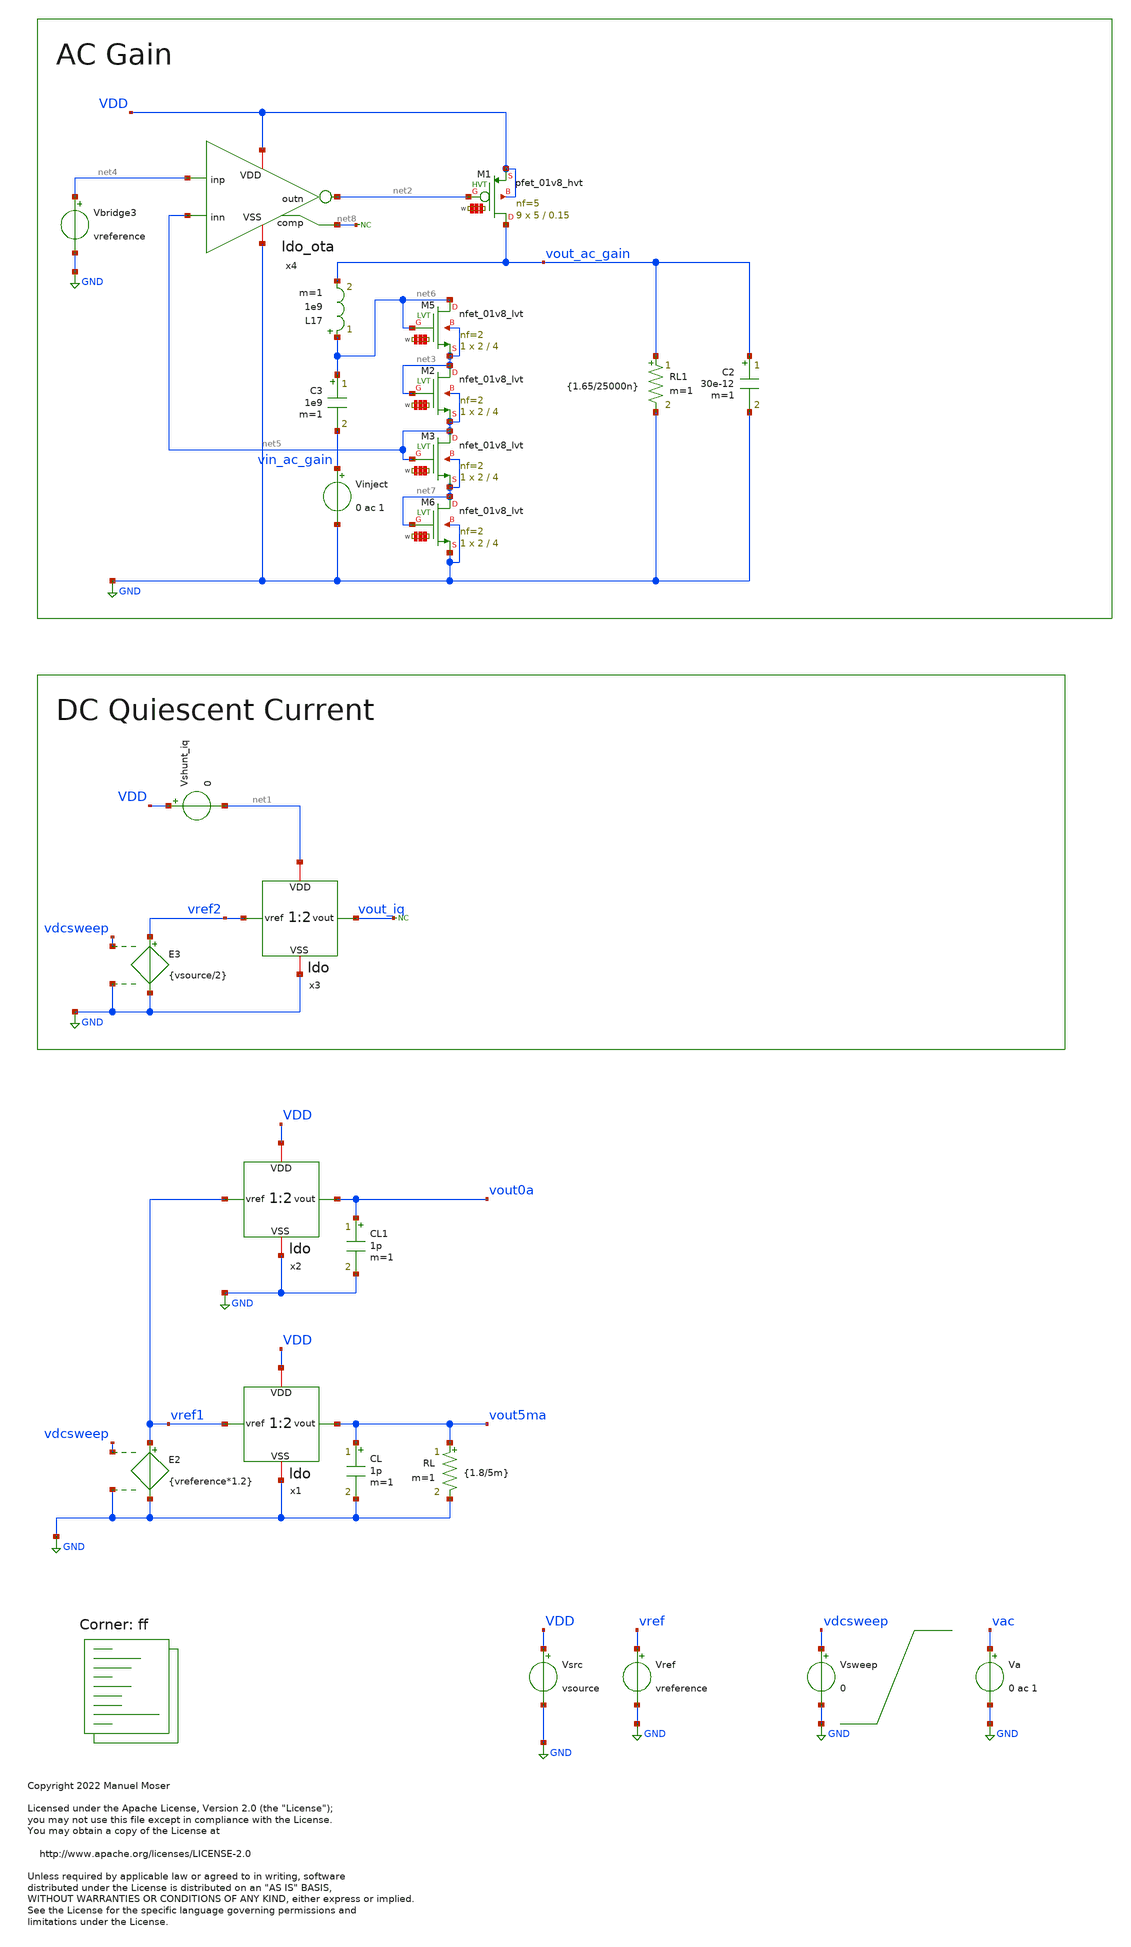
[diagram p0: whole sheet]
** sch_path: xschem/ldo_tb.sch
* Copyright 2022 Manuel Moser
* Licensed under the Apache License, Version 2.0 (the "License");
**.subckt ldo_tb
Vref vref GND vreference
Vsrc VDD GND vsource
Va vac GND 0 ac 1
CL vout5ma GND 1p m=1
RL vout5ma GND {1.8/5m} m=1
x1 VDD vref1 vout5ma GND ldo
CL1 vout0a GND 1p m=1
x2 VDD vref1 vout0a GND ldo
Vsweep vdcsweep GND 0
E2 vref1 GND vdcsweep GND {vreference*1.2}
x3 net1 vref2 vout_iq GND ldo
Vshunt_iq VDD net1 0
E3 vref2 GND vdcsweep GND {vsource/2}
* noconn vout_iq
x4 VDD net4 net2 net5 GND net8 ldo_ota
XM1 vout_ac_gain net2 VDD VDD sky130_fd_pr__pfet_01v8_hvt L=0.15 W='5 * 5 ' nf=5 ad='int((nf+1)/2) * W / nf * 0.29'
+ as='int((nf+2)/2) * W / nf * 0.29' pd='2*int((nf+1)/2) * (W / nf + 0.29)' ps='2*int((nf+2)/2) * (W / nf + 0.29)'
+ nrd='0.29 / W ' nrs='0.29 / W ' sa=0 sb=0 sd=0 mult=9 m=9
XM5 net6 net6 net3 net3 sky130_fd_pr__nfet_01v8_lvt L=4 W='2 * 2 ' nf=2 ad='int((nf+1)/2) * W/nf * 0.29'
+ as='int((nf+2)/2) * W/nf * 0.29' pd='2*int((nf+1)/2) * (W/nf + 0.29)' ps='2*int((nf+2)/2) * (W/nf + 0.29)'
+ nrd='0.29 / W' nrs='0.29 / W' sa=0 sb=0 sd=0 mult=1 m=1
XM2 net3 net3 net5 net5 sky130_fd_pr__nfet_01v8_lvt L=4 W='2 * 2 ' nf=2 ad='int((nf+1)/2) * W/nf * 0.29'
+ as='int((nf+2)/2) * W/nf * 0.29' pd='2*int((nf+1)/2) * (W/nf + 0.29)' ps='2*int((nf+2)/2) * (W/nf + 0.29)'
+ nrd='0.29 / W' nrs='0.29 / W' sa=0 sb=0 sd=0 mult=1 m=1
XM3 net5 net5 net7 net7 sky130_fd_pr__nfet_01v8_lvt L=4 W='2 * 2 ' nf=2 ad='int((nf+1)/2) * W/nf * 0.29'
+ as='int((nf+2)/2) * W/nf * 0.29' pd='2*int((nf+1)/2) * (W/nf + 0.29)' ps='2*int((nf+2)/2) * (W/nf + 0.29)'
+ nrd='0.29 / W' nrs='0.29 / W' sa=0 sb=0 sd=0 mult=1 m=1
XM6 net7 net7 GND GND sky130_fd_pr__nfet_01v8_lvt L=4 W='2 * 2 ' nf=2 ad='int((nf+1)/2) * W/nf * 0.29'
+ as='int((nf+2)/2) * W/nf * 0.29' pd='2*int((nf+1)/2) * (W/nf + 0.29)' ps='2*int((nf+2)/2) * (W/nf + 0.29)'
+ nrd='0.29 / W' nrs='0.29 / W' sa=0 sb=0 sd=0 mult=1 m=1
L17 net6 vout_ac_gain 1e9 m=1
C3 net6 vin_ac_gain 1e9 m=1
Vinject vin_ac_gain GND 0 ac 1
Vbridge3 net4 GND vreference
RL1 vout_ac_gain GND {1.65/25000n} m=1
C2 vout_ac_gain GND 30e-12 m=1
* noconn #net8
**** begin user architecture code



.temp 27
*.option gmin = 1e-16
.option RSHUNT=1E15
.option method = gear

.param vsource = 1.8
.param vdrop = 0.15
.param vreference = {(vsource-vdrop)/2}

.save all
.options savecurrents

.control
set num_threads = 12
write results_ldo.raw
set appendwrite

repeat 1
 reset

dc vsweep 0 1 0.01 temp -30 60 90
write results_ldo.raw   vref1 vout5ma vout0a x1.vota x1.vfb
+ @m.x1.xm5.msky130_fd_pr__nfet_01v8_lvt[id]  vref2 i(vshunt_iq) vout_ac_gain

ac dec 10 1 10meg
write results_ldo.raw vout_ac_gain

*pz vinject gnd vout_ac_gain gnd vol pz


end

.endc




.lib $::SKYWATER_MODELS/sky130.lib.spice ff
**** end user architecture code
**.ends

* expanding   symbol:  ldo.sym # of pins=4
** sym_path: xschem/ldo.sym
** sch_path: xschem/ldo.sch
.subckt ldo VDD vref vout VSS
*.ipin vref
*.iopin VDD
*.iopin VSS
*.opin vout
x1 VDD vref vota vfb VSS ldo_ota
XM1 vout vota VDD VDD sky130_fd_pr__pfet_01v8_hvt L=0.15 W='5 * 5 ' nf=5 ad='int((nf+1)/2) * W / nf * 0.29'
+ as='int((nf+2)/2) * W / nf * 0.29' pd='2*int((nf+1)/2) * (W / nf + 0.29)' ps='2*int((nf+2)/2) * (W / nf + 0.29)'
+ nrd='0.29 / W ' nrs='0.29 / W ' sa=0 sb=0 sd=0 mult=9 m=9
XM5 vout vout net1 net1 sky130_fd_pr__nfet_01v8_lvt L=4 W='2 * 2 ' nf=2 ad='int((nf+1)/2) * W/nf * 0.29'
+ as='int((nf+2)/2) * W/nf * 0.29' pd='2*int((nf+1)/2) * (W/nf + 0.29)' ps='2*int((nf+2)/2) * (W/nf + 0.29)'
+ nrd='0.29 / W' nrs='0.29 / W' sa=0 sb=0 sd=0 mult=1 m=1
XM2 net1 net1 vfb vfb sky130_fd_pr__nfet_01v8_lvt L=4 W='2 * 2 ' nf=2 ad='int((nf+1)/2) * W/nf * 0.29'
+ as='int((nf+2)/2) * W/nf * 0.29' pd='2*int((nf+1)/2) * (W/nf + 0.29)' ps='2*int((nf+2)/2) * (W/nf + 0.29)'
+ nrd='0.29 / W' nrs='0.29 / W' sa=0 sb=0 sd=0 mult=1 m=1
XM3 vfb vfb net2 net2 sky130_fd_pr__nfet_01v8_lvt L=4 W='2 * 2 ' nf=2 ad='int((nf+1)/2) * W/nf * 0.29'
+ as='int((nf+2)/2) * W/nf * 0.29' pd='2*int((nf+1)/2) * (W/nf + 0.29)' ps='2*int((nf+2)/2) * (W/nf + 0.29)'
+ nrd='0.29 / W' nrs='0.29 / W' sa=0 sb=0 sd=0 mult=1 m=1
XM6 net2 net2 VSS VSS sky130_fd_pr__nfet_01v8_lvt L=4 W='2 * 2 ' nf=2 ad='int((nf+1)/2) * W/nf * 0.29'
+ as='int((nf+2)/2) * W/nf * 0.29' pd='2*int((nf+1)/2) * (W/nf + 0.29)' ps='2*int((nf+2)/2) * (W/nf + 0.29)'
+ nrd='0.29 / W' nrs='0.29 / W' sa=0 sb=0 sd=0 mult=1 m=1
.ends


* expanding   symbol:  ldo_ota.sym # of pins=6
** sym_path: xschem/ldo_ota.sym
** sch_path: xschem/ldo_ota.sch
.subckt ldo_ota VDD inp outn inn VSS comp
*.iopin VDD
*.iopin VSS
*.ipin inp
*.ipin inn
*.opin outn
*.opin comp
x2 bias2 VDD VSS bias1 ldo_isource
XM10 net1 bias2 VDD VDD sky130_fd_pr__pfet_01v8_lvt L=8 W='0.55 * 1 ' nf=1 ad='int((nf+1)/2) * W / nf * 0.29'
+ as='int((nf+2)/2) * W / nf * 0.29' pd='2*int((nf+1)/2) * (W / nf + 0.29)' ps='2*int((nf+2)/2) * (W / nf + 0.29)'
+ nrd='0.29 / W ' nrs='0.29 / W ' sa=0 sb=0 sd=0 mult=1 m=1
XM12 bias2 bias2 net1 VDD sky130_fd_pr__pfet_01v8_lvt L=1 W='3 * 3 ' nf=3 ad='int((nf+1)/2) * W / nf * 0.29'
+ as='int((nf+2)/2) * W / nf * 0.29' pd='2*int((nf+1)/2) * (W / nf + 0.29)' ps='2*int((nf+2)/2) * (W / nf + 0.29)'
+ nrd='0.29 / W ' nrs='0.29 / W ' sa=0 sb=0 sd=0 mult=1 m=1
XM1 net2 bias1 VDD VDD sky130_fd_pr__pfet_01v8_lvt L=8 W='0.55 * 4 ' nf=4 ad='int((nf+1)/2) * W / nf * 0.29'
+ as='int((nf+2)/2) * W / nf * 0.29' pd='2*int((nf+1)/2) * (W / nf + 0.29)' ps='2*int((nf+2)/2) * (W / nf + 0.29)'
+ nrd='0.29 / W ' nrs='0.29 / W ' sa=0 sb=0 sd=0 mult=1 m=1
XM2 bias1 bias2 net2 VDD sky130_fd_pr__pfet_01v8_lvt L=1 W='3 * 3 ' nf=3 ad='int((nf+1)/2) * W / nf * 0.29'
+ as='int((nf+2)/2) * W / nf * 0.29' pd='2*int((nf+1)/2) * (W / nf + 0.29)' ps='2*int((nf+2)/2) * (W / nf + 0.29)'
+ nrd='0.29 / W ' nrs='0.29 / W ' sa=0 sb=0 sd=0 mult=1 m=1
XM3 net3 bias1 VDD VDD sky130_fd_pr__pfet_01v8_lvt L=8 W='0.55 * 4 ' nf=4 ad='int((nf+1)/2) * W / nf * 0.29'
+ as='int((nf+2)/2) * W / nf * 0.29' pd='2*int((nf+1)/2) * (W / nf + 0.29)' ps='2*int((nf+2)/2) * (W / nf + 0.29)'
+ nrd='0.29 / W ' nrs='0.29 / W ' sa=0 sb=0 sd=0 mult=1 m=1
XM4 bias3 bias2 net3 VDD sky130_fd_pr__pfet_01v8_lvt L=1 W='3 * 3 ' nf=3 ad='int((nf+1)/2) * W / nf * 0.29'
+ as='int((nf+2)/2) * W / nf * 0.29' pd='2*int((nf+1)/2) * (W / nf + 0.29)' ps='2*int((nf+2)/2) * (W / nf + 0.29)'
+ nrd='0.29 / W ' nrs='0.29 / W ' sa=0 sb=0 sd=0 mult=1 m=1
XM5 net4 bias1 VDD VDD sky130_fd_pr__pfet_01v8_lvt L=8 W='0.55 * 4 ' nf=4 ad='int((nf+1)/2) * W / nf * 0.29'
+ as='int((nf+2)/2) * W / nf * 0.29' pd='2*int((nf+1)/2) * (W / nf + 0.29)' ps='2*int((nf+2)/2) * (W / nf + 0.29)'
+ nrd='0.29 / W ' nrs='0.29 / W ' sa=0 sb=0 sd=0 mult=1 m=1
XM8 bias4 bias2 net4 VDD sky130_fd_pr__pfet_01v8_lvt L=1 W='3 * 3 ' nf=3 ad='int((nf+1)/2) * W / nf * 0.29'
+ as='int((nf+2)/2) * W / nf * 0.29' pd='2*int((nf+1)/2) * (W / nf + 0.29)' ps='2*int((nf+2)/2) * (W / nf + 0.29)'
+ nrd='0.29 / W ' nrs='0.29 / W ' sa=0 sb=0 sd=0 mult=1 m=1
XM9 bias3 bias3 net5 VSS sky130_fd_pr__nfet_01v8_lvt L=0.5 W='1 * 2 ' nf=2 ad='int((nf+1)/2) * W / nf * 0.29'
+ as='int((nf+2)/2) * W / nf * 0.29' pd='2*int((nf+1)/2) * (W / nf + 0.29)' ps='2*int((nf+2)/2) * (W / nf + 0.29)'
+ nrd='0.29 / W ' nrs='0.29 / W ' sa=0 sb=0 sd=0 mult=1 m=1
XM11 net5 bias3 net10 VSS sky130_fd_pr__nfet_01v8 L=8 W='0.42 * 1 ' nf=1 ad='int((nf+1)/2) * W / nf * 0.29'
+ as='int((nf+2)/2) * W / nf * 0.29' pd='2*int((nf+1)/2) * (W / nf + 0.29)' ps='2*int((nf+2)/2) * (W / nf + 0.29)'
+ nrd='0.29 / W ' nrs='0.29 / W ' sa=0 sb=0 sd=0 mult=1 m=1
XM13 bias4 bias3 net6 VSS sky130_fd_pr__nfet_01v8_lvt L=0.5 W='1 * 2 ' nf=2 ad='int((nf+1)/2) * W / nf * 0.29'
+ as='int((nf+2)/2) * W / nf * 0.29' pd='2*int((nf+1)/2) * (W / nf + 0.29)' ps='2*int((nf+2)/2) * (W / nf + 0.29)'
+ nrd='0.29 / W ' nrs='0.29 / W ' sa=0 sb=0 sd=0 mult=1 m=1
XM14 net6 bias4 net7 VSS sky130_fd_pr__nfet_01v8 L=8 W='0.42 * 3 ' nf=3 ad='int((nf+1)/2) * W / nf * 0.29'
+ as='int((nf+2)/2) * W / nf * 0.29' pd='2*int((nf+1)/2) * (W / nf + 0.29)' ps='2*int((nf+2)/2) * (W / nf + 0.29)'
+ nrd='0.29 / W ' nrs='0.29 / W ' sa=0 sb=0 sd=0 mult=1 m=1
XM6 net7 bias4 net8 VSS sky130_fd_pr__nfet_01v8 L=8 W='0.42 * 3 ' nf=3 ad='int((nf+1)/2) * W / nf * 0.29'
+ as='int((nf+2)/2) * W / nf * 0.29' pd='2*int((nf+1)/2) * (W / nf + 0.29)' ps='2*int((nf+2)/2) * (W / nf + 0.29)'
+ nrd='0.29 / W ' nrs='0.29 / W ' sa=0 sb=0 sd=0 mult=1 m=1
XM7 net10 bias3 net9 VSS sky130_fd_pr__nfet_01v8 L=8 W='0.42 * 1 ' nf=1 ad='int((nf+1)/2) * W / nf * 0.29'
+ as='int((nf+2)/2) * W / nf * 0.29' pd='2*int((nf+1)/2) * (W / nf + 0.29)' ps='2*int((nf+2)/2) * (W / nf + 0.29)'
+ nrd='0.29 / W ' nrs='0.29 / W ' sa=0 sb=0 sd=0 mult=1 m=1
x1 VDD inp inn bias1 bias2 bias3 outn VSS bias4 comp ldo_fc_n
XM15 net9 bias3 net11 VSS sky130_fd_pr__nfet_01v8 L=8 W='0.42 * 1 ' nf=1 ad='int((nf+1)/2) * W / nf * 0.29'
+ as='int((nf+2)/2) * W / nf * 0.29' pd='2*int((nf+1)/2) * (W / nf + 0.29)' ps='2*int((nf+2)/2) * (W / nf + 0.29)'
+ nrd='0.29 / W ' nrs='0.29 / W ' sa=0 sb=0 sd=0 mult=1 m=1
XM16 net8 bias4 net12 VSS sky130_fd_pr__nfet_01v8 L=8 W='0.42 * 3 ' nf=3 ad='int((nf+1)/2) * W / nf * 0.29'
+ as='int((nf+2)/2) * W / nf * 0.29' pd='2*int((nf+1)/2) * (W / nf + 0.29)' ps='2*int((nf+2)/2) * (W / nf + 0.29)'
+ nrd='0.29 / W ' nrs='0.29 / W ' sa=0 sb=0 sd=0 mult=1 m=1
XM17 net12 bias4 VSS VSS sky130_fd_pr__nfet_01v8 L=8 W='0.42 * 3 ' nf=3 ad='int((nf+1)/2) * W / nf * 0.29'
+ as='int((nf+2)/2) * W / nf * 0.29' pd='2*int((nf+1)/2) * (W / nf + 0.29)' ps='2*int((nf+2)/2) * (W / nf + 0.29)'
+ nrd='0.29 / W ' nrs='0.29 / W ' sa=0 sb=0 sd=0 mult=1 m=1
XM18 net11 bias3 VSS VSS sky130_fd_pr__nfet_01v8 L=8 W='0.42 * 1 ' nf=1 ad='int((nf+1)/2) * W / nf * 0.29'
+ as='int((nf+2)/2) * W / nf * 0.29' pd='2*int((nf+1)/2) * (W / nf + 0.29)' ps='2*int((nf+2)/2) * (W / nf + 0.29)'
+ nrd='0.29 / W ' nrs='0.29 / W ' sa=0 sb=0 sd=0 mult=1 m=1
.ends


* expanding   symbol:  ldo_isource.sym # of pins=4
** sym_path: xschem/ldo_isource.sym
** sch_path: xschem/ldo_isource.sch
.subckt ldo_isource curr_n1 VDD VSS curr_n2
*.iopin VDD
*.iopin VSS
*.ipin curr_n1
*.ipin curr_n2
XMP2 VGP VGP net4 VDD sky130_fd_pr__pfet_01v8_lvt L=8 W='0.55 * 7 ' nf=7 ad='int((nf+1)/2) * W / nf * 0.29'
+ as='int((nf+2)/2) * W / nf * 0.29' pd='2*int((nf+1)/2) * (W / nf + 0.29)' ps='2*int((nf+2)/2) * (W / nf + 0.29)'
+ nrd='0.29 / W ' nrs='0.29 / W ' sa=0 sb=0 sd=0 mult=1 m=1
XMP1 VGN VGP net3 VDD sky130_fd_pr__pfet_01v8_lvt L=8 W='0.55 * 7 ' nf=7 ad='int((nf+1)/2) * W / nf * 0.29'
+ as='int((nf+2)/2) * W / nf * 0.29' pd='2*int((nf+1)/2) * (W / nf + 0.29)' ps='2*int((nf+2)/2) * (W / nf + 0.29)'
+ nrd='0.29 / W ' nrs='0.29 / W ' sa=0 sb=0 sd=0 mult=1 m=1
XMN1 VGN VGN net1 VSS sky130_fd_pr__nfet_01v8_lvt L=8 W='7 * 1 ' nf=1 ad='int((nf+1)/2) * W / nf * 0.29'
+ as='int((nf+2)/2) * W / nf * 0.29' pd='2*int((nf+1)/2) * (W / nf + 0.29)' ps='2*int((nf+2)/2) * (W / nf + 0.29)'
+ nrd='0.29 / W ' nrs='0.29 / W ' sa=0 sb=0 sd=0 mult=1 m=1
XMN2 VGP VGN net2 VSS sky130_fd_pr__nfet_01v8_lvt L=8 W='7 * 1 ' nf=1 ad='int((nf+1)/2) * W / nf * 0.29'
+ as='int((nf+2)/2) * W / nf * 0.29' pd='2*int((nf+1)/2) * (W / nf + 0.29)' ps='2*int((nf+2)/2) * (W / nf + 0.29)'
+ nrd='0.29 / W ' nrs='0.29 / W ' sa=0 sb=0 sd=0 mult=5 m=5
XMN3 net1 VGN VSS VSS sky130_fd_pr__nfet_01v8_lvt L=8 W='7 * 1 ' nf=1 ad='int((nf+1)/2) * W / nf * 0.29'
+ as='int((nf+2)/2) * W / nf * 0.29' pd='2*int((nf+1)/2) * (W / nf + 0.29)' ps='2*int((nf+2)/2) * (W / nf + 0.29)'
+ nrd='0.29 / W ' nrs='0.29 / W ' sa=0 sb=0 sd=0 mult=1 m=1
XMN4 net2 VGN Vref VSS sky130_fd_pr__nfet_01v8_lvt L=8 W='7 * 1 ' nf=1 ad='int((nf+1)/2) * W / nf * 0.29'
+ as='int((nf+2)/2) * W / nf * 0.29' pd='2*int((nf+1)/2) * (W / nf + 0.29)' ps='2*int((nf+2)/2) * (W / nf + 0.29)'
+ nrd='0.29 / W ' nrs='0.29 / W ' sa=0 sb=0 sd=0 mult=5 m=5
XMP4 net3 VGP VDD VDD sky130_fd_pr__pfet_01v8_lvt L=8 W='0.55 * 7 ' nf=7 ad='int((nf+1)/2) * W / nf * 0.29'
+ as='int((nf+2)/2) * W / nf * 0.29' pd='2*int((nf+1)/2) * (W / nf + 0.29)' ps='2*int((nf+2)/2) * (W / nf + 0.29)'
+ nrd='0.29 / W ' nrs='0.29 / W ' sa=0 sb=0 sd=0 mult=1 m=1
XMP5 net4 VGP VDD VDD sky130_fd_pr__pfet_01v8_lvt L=8 W='0.55 * 7 ' nf=7 ad='int((nf+1)/2) * W / nf * 0.29'
+ as='int((nf+2)/2) * W / nf * 0.29' pd='2*int((nf+1)/2) * (W / nf + 0.29)' ps='2*int((nf+2)/2) * (W / nf + 0.29)'
+ nrd='0.29 / W ' nrs='0.29 / W ' sa=0 sb=0 sd=0 mult=1 m=1
XMP3 Vrefgate VGP net19 VDD sky130_fd_pr__pfet_01v8_lvt L=8 W='0.55 * 7 ' nf=7 ad='int((nf+1)/2) * W / nf * 0.29'
+ as='int((nf+2)/2) * W / nf * 0.29' pd='2*int((nf+1)/2) * (W / nf + 0.29)' ps='2*int((nf+2)/2) * (W / nf + 0.29)'
+ nrd='0.29 / W ' nrs='0.29 / W ' sa=0 sb=0 sd=0 mult=1 m=1
XM2 net5 Vrefgate net6 VSS sky130_fd_pr__nfet_01v8 L=4 W='1 * 1 ' nf=1 ad='int((nf+1)/2) * W / nf * 0.29'
+ as='int((nf+2)/2) * W / nf * 0.29' pd='2*int((nf+1)/2) * (W / nf + 0.29)' ps='2*int((nf+2)/2) * (W / nf + 0.29)'
+ nrd='0.29 / W ' nrs='0.29 / W ' sa=0 sb=0 sd=0 mult=1 m=1
XM3 net8 Vrefgate VSS VSS sky130_fd_pr__nfet_01v8 L=4 W='1 * 1 ' nf=1 ad='int((nf+1)/2) * W / nf * 0.29'
+ as='int((nf+2)/2) * W / nf * 0.29' pd='2*int((nf+1)/2) * (W / nf + 0.29)' ps='2*int((nf+2)/2) * (W / nf + 0.29)'
+ nrd='0.29 / W ' nrs='0.29 / W ' sa=0 sb=0 sd=0 mult=1 m=1
XM1 net7 Vrefgate net8 VSS sky130_fd_pr__nfet_01v8 L=4 W='1 * 1 ' nf=1 ad='int((nf+1)/2) * W / nf * 0.29'
+ as='int((nf+2)/2) * W / nf * 0.29' pd='2*int((nf+1)/2) * (W / nf + 0.29)' ps='2*int((nf+2)/2) * (W / nf + 0.29)'
+ nrd='0.29 / W ' nrs='0.29 / W ' sa=0 sb=0 sd=0 mult=1 m=1
XM4 net6 Vrefgate net7 VSS sky130_fd_pr__nfet_01v8 L=4 W='1 * 1 ' nf=1 ad='int((nf+1)/2) * W / nf * 0.29'
+ as='int((nf+2)/2) * W / nf * 0.29' pd='2*int((nf+1)/2) * (W / nf + 0.29)' ps='2*int((nf+2)/2) * (W / nf + 0.29)'
+ nrd='0.29 / W ' nrs='0.29 / W ' sa=0 sb=0 sd=0 mult=1 m=1
XMN5 net10 Vrefgate VSS VSS sky130_fd_pr__nfet_01v8_lvt L=4 W='1 * 1 ' nf=1 ad='int((nf+1)/2) * W / nf * 0.29'
+ as='int((nf+2)/2) * W / nf * 0.29' pd='2*int((nf+1)/2) * (W / nf + 0.29)' ps='2*int((nf+2)/2) * (W / nf + 0.29)'
+ nrd='0.29 / W ' nrs='0.29 / W ' sa=0 sb=0 sd=0 mult=1 m=1
XMN6 net14 Vrefgate net9 VSS sky130_fd_pr__nfet_01v8_lvt L=4 W='1 * 1 ' nf=1 ad='int((nf+1)/2) * W / nf * 0.29'
+ as='int((nf+2)/2) * W / nf * 0.29' pd='2*int((nf+1)/2) * (W / nf + 0.29)' ps='2*int((nf+2)/2) * (W / nf + 0.29)'
+ nrd='0.29 / W ' nrs='0.29 / W ' sa=0 sb=0 sd=0 mult=1 m=1
XMN9 net16 Vrefgate net14 VSS sky130_fd_pr__nfet_01v8_lvt L=4 W='1 * 1 ' nf=1 ad='int((nf+1)/2) * W / nf * 0.29'
+ as='int((nf+2)/2) * W / nf * 0.29' pd='2*int((nf+1)/2) * (W / nf + 0.29)' ps='2*int((nf+2)/2) * (W / nf + 0.29)'
+ nrd='0.29 / W ' nrs='0.29 / W ' sa=0 sb=0 sd=0 mult=1 m=1
XM5 Vrefgate Vrefgate net5 VSS sky130_fd_pr__nfet_01v8 L=4 W='1 * 1 ' nf=1 ad='int((nf+1)/2) * W / nf * 0.29'
+ as='int((nf+2)/2) * W / nf * 0.29' pd='2*int((nf+1)/2) * (W / nf + 0.29)' ps='2*int((nf+2)/2) * (W / nf + 0.29)'
+ nrd='0.29 / W ' nrs='0.29 / W ' sa=0 sb=0 sd=0 mult=1 m=1
XMN10 net11 Vrefgate net10 VSS sky130_fd_pr__nfet_01v8_lvt L=4 W='1 * 1 ' nf=1 ad='int((nf+1)/2) * W / nf * 0.29'
+ as='int((nf+2)/2) * W / nf * 0.29' pd='2*int((nf+1)/2) * (W / nf + 0.29)' ps='2*int((nf+2)/2) * (W / nf + 0.29)'
+ nrd='0.29 / W ' nrs='0.29 / W ' sa=0 sb=0 sd=0 mult=1 m=1
XMN11 net12 Vrefgate net11 VSS sky130_fd_pr__nfet_01v8_lvt L=4 W='1 * 1 ' nf=1 ad='int((nf+1)/2) * W / nf * 0.29'
+ as='int((nf+2)/2) * W / nf * 0.29' pd='2*int((nf+1)/2) * (W / nf + 0.29)' ps='2*int((nf+2)/2) * (W / nf + 0.29)'
+ nrd='0.29 / W ' nrs='0.29 / W ' sa=0 sb=0 sd=0 mult=1 m=1
XMN12 net13 Vrefgate net12 VSS sky130_fd_pr__nfet_01v8_lvt L=4 W='1 * 1 ' nf=1 ad='int((nf+1)/2) * W / nf * 0.29'
+ as='int((nf+2)/2) * W / nf * 0.29' pd='2*int((nf+1)/2) * (W / nf + 0.29)' ps='2*int((nf+2)/2) * (W / nf + 0.29)'
+ nrd='0.29 / W ' nrs='0.29 / W ' sa=0 sb=0 sd=0 mult=1 m=1
XMN13 net9 Vrefgate net13 VSS sky130_fd_pr__nfet_01v8_lvt L=4 W='1 * 1 ' nf=1 ad='int((nf+1)/2) * W / nf * 0.29'
+ as='int((nf+2)/2) * W / nf * 0.29' pd='2*int((nf+1)/2) * (W / nf + 0.29)' ps='2*int((nf+2)/2) * (W / nf + 0.29)'
+ nrd='0.29 / W ' nrs='0.29 / W ' sa=0 sb=0 sd=0 mult=1 m=1
XMN7 net18 Vrefgate net15 VSS sky130_fd_pr__nfet_01v8_lvt L=4 W='1 * 1 ' nf=1 ad='int((nf+1)/2) * W / nf * 0.29'
+ as='int((nf+2)/2) * W / nf * 0.29' pd='2*int((nf+1)/2) * (W / nf + 0.29)' ps='2*int((nf+2)/2) * (W / nf + 0.29)'
+ nrd='0.29 / W ' nrs='0.29 / W ' sa=0 sb=0 sd=0 mult=1 m=1
XMN8 Vref Vrefgate net18 VSS sky130_fd_pr__nfet_01v8_lvt L=4 W='1 * 1 ' nf=1 ad='int((nf+1)/2) * W / nf * 0.29'
+ as='int((nf+2)/2) * W / nf * 0.29' pd='2*int((nf+1)/2) * (W / nf + 0.29)' ps='2*int((nf+2)/2) * (W / nf + 0.29)'
+ nrd='0.29 / W ' nrs='0.29 / W ' sa=0 sb=0 sd=0 mult=1 m=1
XMN14 net17 Vrefgate net16 VSS sky130_fd_pr__nfet_01v8_lvt L=4 W='1 * 1 ' nf=1 ad='int((nf+1)/2) * W / nf * 0.29'
+ as='int((nf+2)/2) * W / nf * 0.29' pd='2*int((nf+1)/2) * (W / nf + 0.29)' ps='2*int((nf+2)/2) * (W / nf + 0.29)'
+ nrd='0.29 / W ' nrs='0.29 / W ' sa=0 sb=0 sd=0 mult=1 m=1
XMN15 net15 Vrefgate net17 VSS sky130_fd_pr__nfet_01v8_lvt L=4 W='1 * 1 ' nf=1 ad='int((nf+1)/2) * W / nf * 0.29'
+ as='int((nf+2)/2) * W / nf * 0.29' pd='2*int((nf+1)/2) * (W / nf + 0.29)' ps='2*int((nf+2)/2) * (W / nf + 0.29)'
+ nrd='0.29 / W ' nrs='0.29 / W ' sa=0 sb=0 sd=0 mult=1 m=1
XMP6 net19 VGP VDD VDD sky130_fd_pr__pfet_01v8_lvt L=8 W='0.55 * 7 ' nf=7 ad='int((nf+1)/2) * W / nf * 0.29'
+ as='int((nf+2)/2) * W / nf * 0.29' pd='2*int((nf+1)/2) * (W / nf + 0.29)' ps='2*int((nf+2)/2) * (W / nf + 0.29)'
+ nrd='0.29 / W ' nrs='0.29 / W ' sa=0 sb=0 sd=0 mult=1 m=1
XMN16 curr_n1 VGN net20 VSS sky130_fd_pr__nfet_01v8_lvt L=8 W='7 * 1 ' nf=1 ad='int((nf+1)/2) * W / nf * 0.29'
+ as='int((nf+2)/2) * W / nf * 0.29' pd='2*int((nf+1)/2) * (W / nf + 0.29)' ps='2*int((nf+2)/2) * (W / nf + 0.29)'
+ nrd='0.29 / W ' nrs='0.29 / W ' sa=0 sb=0 sd=0 mult=1 m=1
XMN17 net20 VGN VSS VSS sky130_fd_pr__nfet_01v8_lvt L=8 W='7 * 1 ' nf=1 ad='int((nf+1)/2) * W / nf * 0.29'
+ as='int((nf+2)/2) * W / nf * 0.29' pd='2*int((nf+1)/2) * (W / nf + 0.29)' ps='2*int((nf+2)/2) * (W / nf + 0.29)'
+ nrd='0.29 / W ' nrs='0.29 / W ' sa=0 sb=0 sd=0 mult=1 m=1
XM6 VGP vstartup VGN VSS sky130_fd_pr__nfet_01v8 L=4 W='1 * 1 ' nf=1 ad='int((nf+1)/2) * W / nf * 0.29'
+ as='int((nf+2)/2) * W / nf * 0.29' pd='2*int((nf+1)/2) * (W / nf + 0.29)' ps='2*int((nf+2)/2) * (W / nf + 0.29)'
+ nrd='0.29 / W ' nrs='0.29 / W ' sa=0 sb=0 sd=0 mult=1 m=1
XM7 vstartup Vrefgate VSS VSS sky130_fd_pr__nfet_01v8 L=4 W='1 * 1 ' nf=1 ad='int((nf+1)/2) * W / nf * 0.29'
+ as='int((nf+2)/2) * W / nf * 0.29' pd='2*int((nf+1)/2) * (W / nf + 0.29)' ps='2*int((nf+2)/2) * (W / nf + 0.29)'
+ nrd='0.29 / W ' nrs='0.29 / W ' sa=0 sb=0 sd=0 mult=1 m=1
XMN18 curr_n2 VGN net21 VSS sky130_fd_pr__nfet_01v8_lvt L=8 W='7 * 1 ' nf=1 ad='int((nf+1)/2) * W / nf * 0.29'
+ as='int((nf+2)/2) * W / nf * 0.29' pd='2*int((nf+1)/2) * (W / nf + 0.29)' ps='2*int((nf+2)/2) * (W / nf + 0.29)'
+ nrd='0.29 / W ' nrs='0.29 / W ' sa=0 sb=0 sd=0 mult=1 m=1
XMN19 net21 VGN VSS VSS sky130_fd_pr__nfet_01v8_lvt L=8 W='7 * 1 ' nf=1 ad='int((nf+1)/2) * W / nf * 0.29'
+ as='int((nf+2)/2) * W / nf * 0.29' pd='2*int((nf+1)/2) * (W / nf + 0.29)' ps='2*int((nf+2)/2) * (W / nf + 0.29)'
+ nrd='0.29 / W ' nrs='0.29 / W ' sa=0 sb=0 sd=0 mult=1 m=1
XC1 VDD vstartup sky130_fd_pr__cap_mim_m3_2 W=4 L=4 MF=1 m=1
.ends


* expanding   symbol:  ldo_fc_n.sym # of pins=10
** sym_path: xschem/ldo_fc_n.sym
** sch_path: xschem/ldo_fc_n.sch
.subckt ldo_fc_n VDD inp inn bias1 bias2 bias3 outn VSS bias4 comp
*.iopin VSS
*.iopin VDD
*.ipin inp
*.ipin inn
*.ipin bias1
*.opin outn
*.ipin bias2
*.ipin bias3
*.ipin bias4
*.opin comp
XMN4 outn bias3 net1 VSS sky130_fd_pr__nfet_01v8_lvt L=0.5 W='1 * 2 ' nf=2 ad='int((nf+1)/2) * W / nf * 0.29'
+ as='int((nf+2)/2) * W / nf * 0.29' pd='2*int((nf+1)/2) * (W / nf + 0.29)' ps='2*int((nf+2)/2) * (W / nf + 0.29)'
+ nrd='0.29 / W ' nrs='0.29 / W ' sa=0 sb=0 sd=0 mult=12 m=12
XMN7 net1 net3 net7 VSS sky130_fd_pr__nfet_01v8 L=8 W='0.42 * 3 ' nf=3 ad='int((nf+1)/2) * W / nf * 0.29'
+ as='int((nf+2)/2) * W / nf * 0.29' pd='2*int((nf+1)/2) * (W / nf + 0.29)' ps='2*int((nf+2)/2) * (W / nf + 0.29)'
+ nrd='0.29 / W ' nrs='0.29 / W ' sa=0 sb=0 sd=0 mult=12 m=12
XMN3 net3 bias3 net2 VSS sky130_fd_pr__nfet_01v8_lvt L=0.5 W='1 * 2 ' nf=2 ad='int((nf+1)/2) * W / nf * 0.29'
+ as='int((nf+2)/2) * W / nf * 0.29' pd='2*int((nf+1)/2) * (W / nf + 0.29)' ps='2*int((nf+2)/2) * (W / nf + 0.29)'
+ nrd='0.29 / W ' nrs='0.29 / W ' sa=0 sb=0 sd=0 mult=12 m=12
XMN6 net2 net3 net6 VSS sky130_fd_pr__nfet_01v8 L=8 W='0.42 * 3 ' nf=3 ad='int((nf+1)/2) * W / nf * 0.29'
+ as='int((nf+2)/2) * W / nf * 0.29' pd='2*int((nf+1)/2) * (W / nf + 0.29)' ps='2*int((nf+2)/2) * (W / nf + 0.29)'
+ nrd='0.29 / W ' nrs='0.29 / W ' sa=0 sb=0 sd=0 mult=12 m=12
XMP4 outn bias2 comp VDD sky130_fd_pr__pfet_01v8_lvt L=1 W='3 * 3 ' nf=3 ad='int((nf+1)/2) * W / nf * 0.29'
+ as='int((nf+2)/2) * W / nf * 0.29' pd='2*int((nf+1)/2) * (W / nf + 0.29)' ps='2*int((nf+2)/2) * (W / nf + 0.29)'
+ nrd='0.29 / W ' nrs='0.29 / W ' sa=0 sb=0 sd=0 mult=12 m=12
XMP2 comp bias1 VDD VDD sky130_fd_pr__pfet_01v8_lvt L=8 W='0.55 * 4 ' nf=4 ad='int((nf+1)/2) * W / nf * 0.29'
+ as='int((nf+2)/2) * W / nf * 0.29' pd='2*int((nf+1)/2) * (W / nf + 0.29)' ps='2*int((nf+2)/2) * (W / nf + 0.29)'
+ nrd='0.29 / W ' nrs='0.29 / W ' sa=0 sb=0 sd=0 mult=19 m=19
XMP3 net3 bias2 net4 VDD sky130_fd_pr__pfet_01v8_lvt L=1 W='3 * 3 ' nf=3 ad='int((nf+1)/2) * W / nf * 0.29'
+ as='int((nf+2)/2) * W / nf * 0.29' pd='2*int((nf+1)/2) * (W / nf + 0.29)' ps='2*int((nf+2)/2) * (W / nf + 0.29)'
+ nrd='0.29 / W ' nrs='0.29 / W ' sa=0 sb=0 sd=0 mult=12 m=12
XMP1 net4 bias1 VDD VDD sky130_fd_pr__pfet_01v8_lvt L=8 W='0.55 * 4 ' nf=4 ad='int((nf+1)/2) * W / nf * 0.29'
+ as='int((nf+2)/2) * W / nf * 0.29' pd='2*int((nf+1)/2) * (W / nf + 0.29)' ps='2*int((nf+2)/2) * (W / nf + 0.29)'
+ nrd='0.29 / W ' nrs='0.29 / W ' sa=0 sb=0 sd=0 mult=19 m=19
XMN5 net15 bias4 net8 VSS sky130_fd_pr__nfet_01v8 L=8 W='0.42 * 3 ' nf=3 ad='int((nf+1)/2) * W / nf * 0.29'
+ as='int((nf+2)/2) * W / nf * 0.29' pd='2*int((nf+1)/2) * (W / nf + 0.29)' ps='2*int((nf+2)/2) * (W / nf + 0.29)'
+ nrd='0.29 / W ' nrs='0.29 / W ' sa=0 sb=0 sd=0 mult=14 m=14
XMN1 net4 inn net5 VSS sky130_fd_pr__nfet_01v8_lvt L=0.5 W='1 * 5 ' nf=5 ad='int((nf+1)/2) * W / nf * 0.29'
+ as='int((nf+2)/2) * W / nf * 0.29' pd='2*int((nf+1)/2) * (W / nf + 0.29)' ps='2*int((nf+2)/2) * (W / nf + 0.29)'
+ nrd='0.29 / W ' nrs='0.29 / W ' sa=0 sb=0 sd=0 mult=1 m=1
XMN2 comp inp net5 VSS sky130_fd_pr__nfet_01v8_lvt L=0.5 W='1 * 5 ' nf=5 ad='int((nf+1)/2) * W / nf * 0.29'
+ as='int((nf+2)/2) * W / nf * 0.29' pd='2*int((nf+1)/2) * (W / nf + 0.29)' ps='2*int((nf+2)/2) * (W / nf + 0.29)'
+ nrd='0.29 / W ' nrs='0.29 / W ' sa=0 sb=0 sd=0 mult=1 m=1
XMN9 net7 net3 net9 VSS sky130_fd_pr__nfet_01v8 L=8 W='0.42 * 3 ' nf=3 ad='int((nf+1)/2) * W / nf * 0.29'
+ as='int((nf+2)/2) * W / nf * 0.29' pd='2*int((nf+1)/2) * (W / nf + 0.29)' ps='2*int((nf+2)/2) * (W / nf + 0.29)'
+ nrd='0.29 / W ' nrs='0.29 / W ' sa=0 sb=0 sd=0 mult=12 m=12
XMN10 net6 net3 net10 VSS sky130_fd_pr__nfet_01v8 L=8 W='0.42 * 3 ' nf=3 ad='int((nf+1)/2) * W / nf * 0.29'
+ as='int((nf+2)/2) * W / nf * 0.29' pd='2*int((nf+1)/2) * (W / nf + 0.29)' ps='2*int((nf+2)/2) * (W / nf + 0.29)'
+ nrd='0.29 / W ' nrs='0.29 / W ' sa=0 sb=0 sd=0 mult=12 m=12
XMN11 net8 bias4 net11 VSS sky130_fd_pr__nfet_01v8 L=8 W='0.42 * 3 ' nf=3 ad='int((nf+1)/2) * W / nf * 0.29'
+ as='int((nf+2)/2) * W / nf * 0.29' pd='2*int((nf+1)/2) * (W / nf + 0.29)' ps='2*int((nf+2)/2) * (W / nf + 0.29)'
+ nrd='0.29 / W ' nrs='0.29 / W ' sa=0 sb=0 sd=0 mult=14 m=14
XMN8 net9 net3 net12 VSS sky130_fd_pr__nfet_01v8 L=8 W='0.42 * 3 ' nf=3 ad='int((nf+1)/2) * W / nf * 0.29'
+ as='int((nf+2)/2) * W / nf * 0.29' pd='2*int((nf+1)/2) * (W / nf + 0.29)' ps='2*int((nf+2)/2) * (W / nf + 0.29)'
+ nrd='0.29 / W ' nrs='0.29 / W ' sa=0 sb=0 sd=0 mult=12 m=12
XMN12 net10 net3 net14 VSS sky130_fd_pr__nfet_01v8 L=8 W='0.42 * 3 ' nf=3 ad='int((nf+1)/2) * W / nf * 0.29'
+ as='int((nf+2)/2) * W / nf * 0.29' pd='2*int((nf+1)/2) * (W / nf + 0.29)' ps='2*int((nf+2)/2) * (W / nf + 0.29)'
+ nrd='0.29 / W ' nrs='0.29 / W ' sa=0 sb=0 sd=0 mult=12 m=12
XMN13 net11 bias4 net13 VSS sky130_fd_pr__nfet_01v8 L=8 W='0.42 * 3 ' nf=3 ad='int((nf+1)/2) * W / nf * 0.29'
+ as='int((nf+2)/2) * W / nf * 0.29' pd='2*int((nf+1)/2) * (W / nf + 0.29)' ps='2*int((nf+2)/2) * (W / nf + 0.29)'
+ nrd='0.29 / W ' nrs='0.29 / W ' sa=0 sb=0 sd=0 mult=14 m=14
XMN14 net12 net3 VSS VSS sky130_fd_pr__nfet_01v8 L=8 W='0.42 * 3 ' nf=3 ad='int((nf+1)/2) * W / nf * 0.29'
+ as='int((nf+2)/2) * W / nf * 0.29' pd='2*int((nf+1)/2) * (W / nf + 0.29)' ps='2*int((nf+2)/2) * (W / nf + 0.29)'
+ nrd='0.29 / W ' nrs='0.29 / W ' sa=0 sb=0 sd=0 mult=12 m=12
XMN15 net14 net3 VSS VSS sky130_fd_pr__nfet_01v8 L=8 W='0.42 * 3 ' nf=3 ad='int((nf+1)/2) * W / nf * 0.29'
+ as='int((nf+2)/2) * W / nf * 0.29' pd='2*int((nf+1)/2) * (W / nf + 0.29)' ps='2*int((nf+2)/2) * (W / nf + 0.29)'
+ nrd='0.29 / W ' nrs='0.29 / W ' sa=0 sb=0 sd=0 mult=12 m=12
XMN16 net13 bias4 VSS VSS sky130_fd_pr__nfet_01v8 L=8 W='0.42 * 3 ' nf=3 ad='int((nf+1)/2) * W / nf * 0.29'
+ as='int((nf+2)/2) * W / nf * 0.29' pd='2*int((nf+1)/2) * (W / nf + 0.29)' ps='2*int((nf+2)/2) * (W / nf + 0.29)'
+ nrd='0.29 / W ' nrs='0.29 / W ' sa=0 sb=0 sd=0 mult=14 m=14
XM9 net5 bias3 net15 VSS sky130_fd_pr__nfet_01v8_lvt L=0.5 W='1 * 2 ' nf=2 ad='int((nf+1)/2) * W / nf * 0.29'
+ as='int((nf+2)/2) * W / nf * 0.29' pd='2*int((nf+1)/2) * (W / nf + 0.29)' ps='2*int((nf+2)/2) * (W / nf + 0.29)'
+ nrd='0.29 / W ' nrs='0.29 / W ' sa=0 sb=0 sd=0 mult=1 m=1
.ends

.GLOBAL GND
.end
